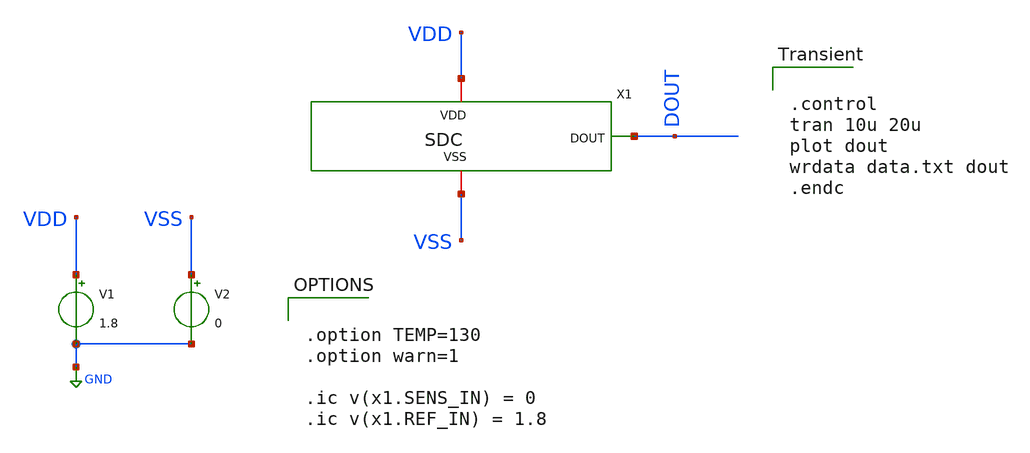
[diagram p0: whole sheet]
** sch_path: samples/cace-tests/SDC/xschem/test_SDCtsens_RINtsweep_9p1_ROrangeext.sch
**.subckt test_SDCtsens_RINtsweep_9p1_ROrangeext
V1 VDD GND 1.8
V2 VSS GND 0
X1 VDD DOUT VSS SDC
**** begin user architecture code

** opencircuitdesign pdks install
.lib $env(PDK_ROOT)/$env(PDK)/libs.tech/ngspice/sky130.lib.spice.tt.red tt
*.lib $env(PDK_ROOT)/$env(PDK)/libs.tech/combined/sky130.lib.spice tt



.control
tran 10u 20u
plot dout
wrdata data.txt dout
.endc



.option TEMP=130
.option warn=1

.ic v(x1.SENS_IN) = 0
.ic v(x1.REF_IN) = 1.8


**** end user architecture code
**.ends
.GLOBAL GND
.end
